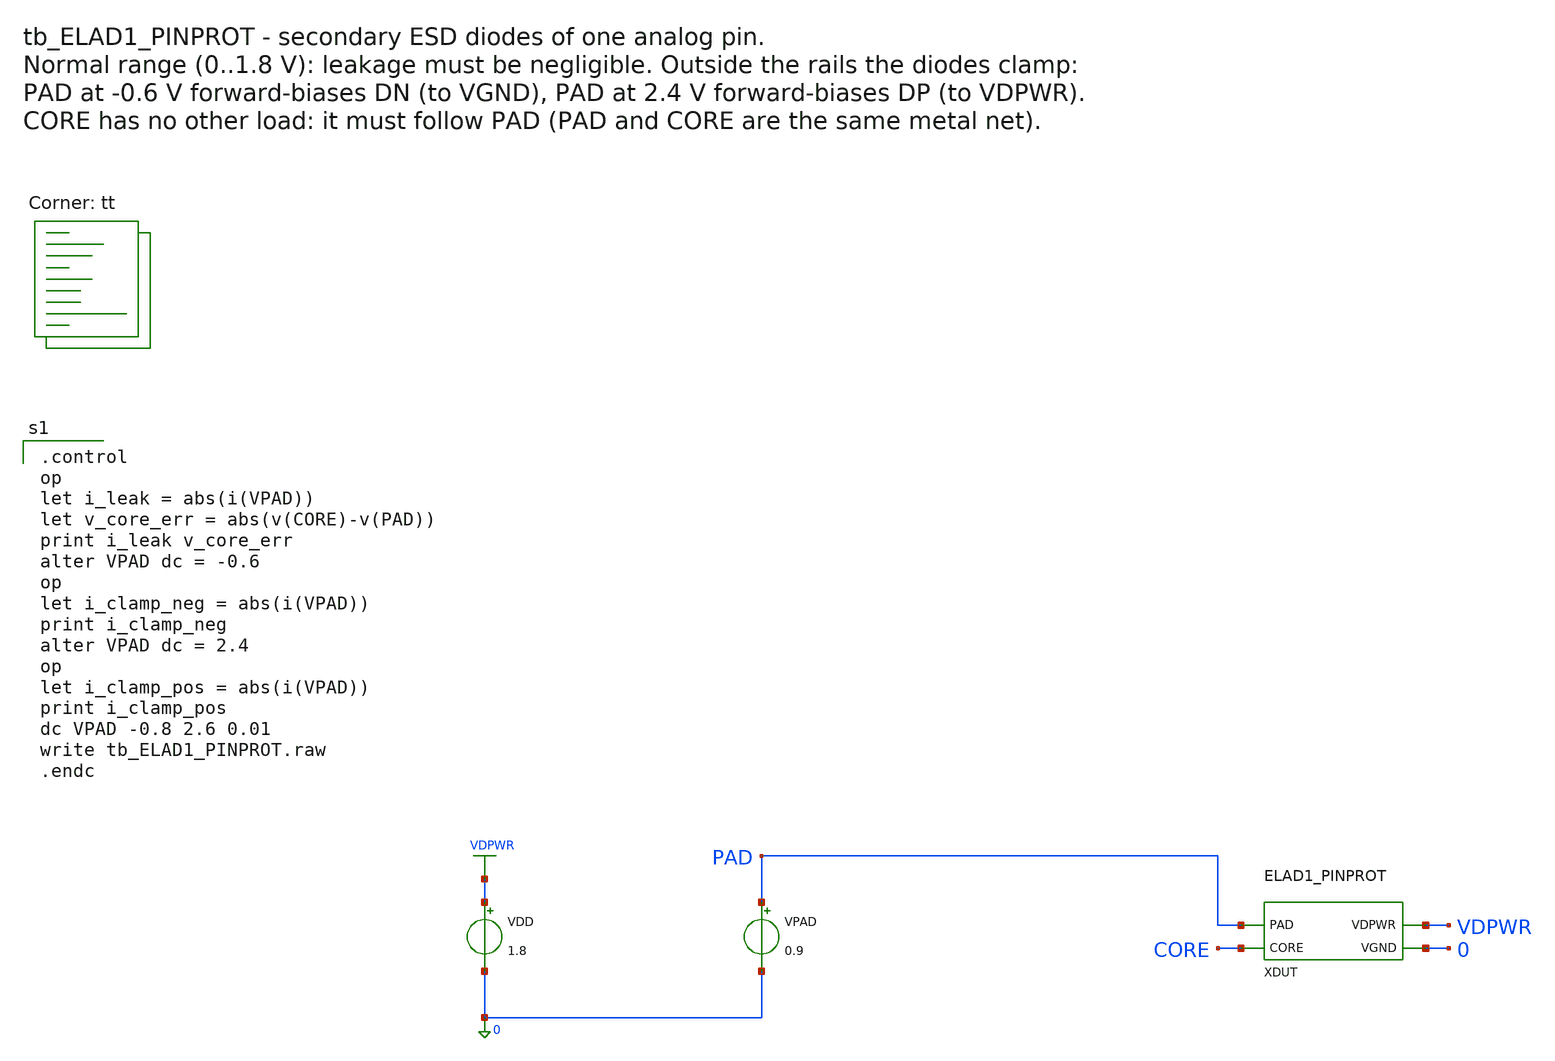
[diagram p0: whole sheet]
** sch_path: cells/ELAD1_PINPROT/schematic/tb_ELAD1_PINPROT.sch
**.subckt tb_ELAD1_PINPROT
VDD VDPWR 0 1.8
VPAD PAD 0 0.9
XDUT PAD CORE VDPWR 0 ELAD1_PINPROT
**** begin user architecture code

.control
op
let i_leak = abs(i(VPAD))
let v_core_err = abs(v(CORE)-v(PAD))
print i_leak v_core_err
alter VPAD dc = -0.6
op
let i_clamp_neg = abs(i(VPAD))
print i_clamp_neg
alter VPAD dc = 2.4
op
let i_clamp_pos = abs(i(VPAD))
print i_clamp_pos
dc VPAD -0.8 2.6 0.01
write tb_ELAD1_PINPROT.raw
.endc

.lib $::SKYWATER_MODELS/sky130.lib.spice tt
**** end user architecture code
**.ends

* expanding   symbol:  ELAD1_PINPROT.sym # of pins=4
** sym_path: cells/ELAD1_PINPROT/schematic/ELAD1_PINPROT.sym
** sch_path: cells/ELAD1_PINPROT/schematic/ELAD1_PINPROT.sch
.subckt ELAD1_PINPROT PAD CORE VDPWR VGND
*.iopin PAD
*.iopin CORE
*.iopin VDPWR
*.iopin VGND
RLINK PAD CORE 0.001 m=1
XDP PAD VDPWR sky130_fd_pr__diode_pd2nw_05v5 area=36 pj=4e6
XDN VGND PAD sky130_fd_pr__diode_pw2nd_05v5 area=36 pj=4e6
.ends

.end
